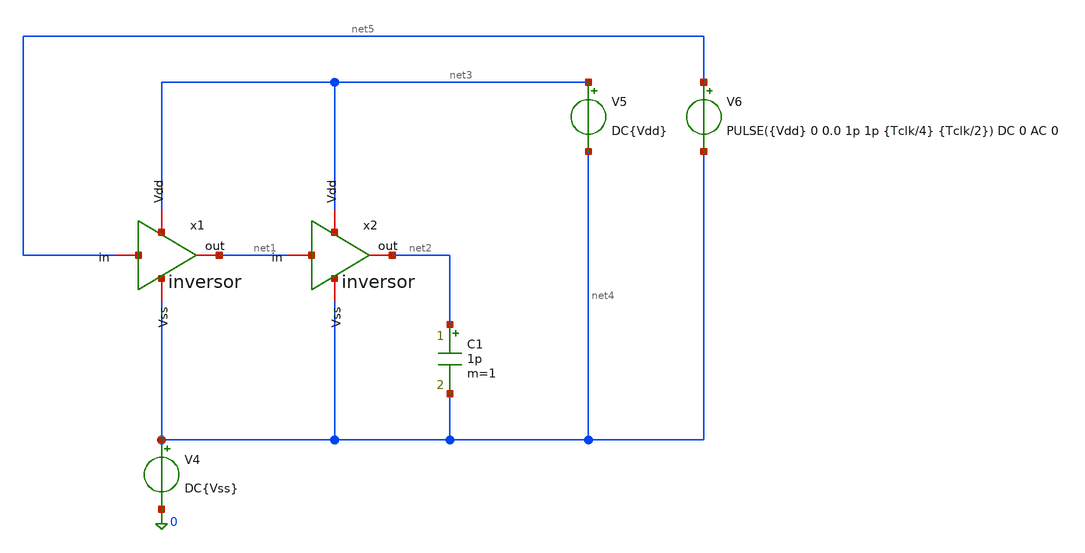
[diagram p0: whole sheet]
** sch_path: verification/testbenches/tb_inversor.sch
**.subckt tb_inversor
x1 net3 net1 net5 net4 inversor
x2 net3 net2 net1 net4 inversor
V4 net4 0 DC{Vss}
V5 net3 net4 DC{Vdd}
V6 net5 net4 PULSE({Vdd} 0 0.0 1p 1p {Tclk/4} {Tclk/2}) DC 0 AC 0
C1 net2 net4 1p m=1
**** begin user architecture code


* Circuit Parameters
.param vdd = 1.2
.param vss = 0.0
.param Tclk = 10n
.options TEMP = 27.0
* Include Models - IHP SG13G2
.lib cornerMOSlv.lib mos_tt
* OP Parameters & Singals to save
.save all
*Simulations
.control
tran 0.01u 100n
setplot tran1
plot v(vin) v(vout)+1.2
reset
dc V6 0 1.2 0.01
setplot dc
plot vin vout ylabel vout xlabel vin
set filetype = ascii
write dcsweep.raw
.endc
.end


**** end user architecture code
**.ends

* expanding   symbol:  blocks/inversor/schematic/inversor.sym # of pins=4
** sym_path: design/blocks/inversor/schematic/inversor.sym
** sch_path: design/blocks/inversor/schematic/inversor.sch
.subckt inversor Vdd out in Vss
*.iopin out
*.iopin Vdd
*.iopin Vss
*.iopin in
XM3 out in Vdd Vdd sg13_lv_pmos w=0.45u l=0.15u ng=1 m=1 mm_ok=1
XM1 out in Vss Vss sg13_lv_nmos w=0.15u l=0.45u ng=1 m=1 mm_ok=1
.ends

.end
